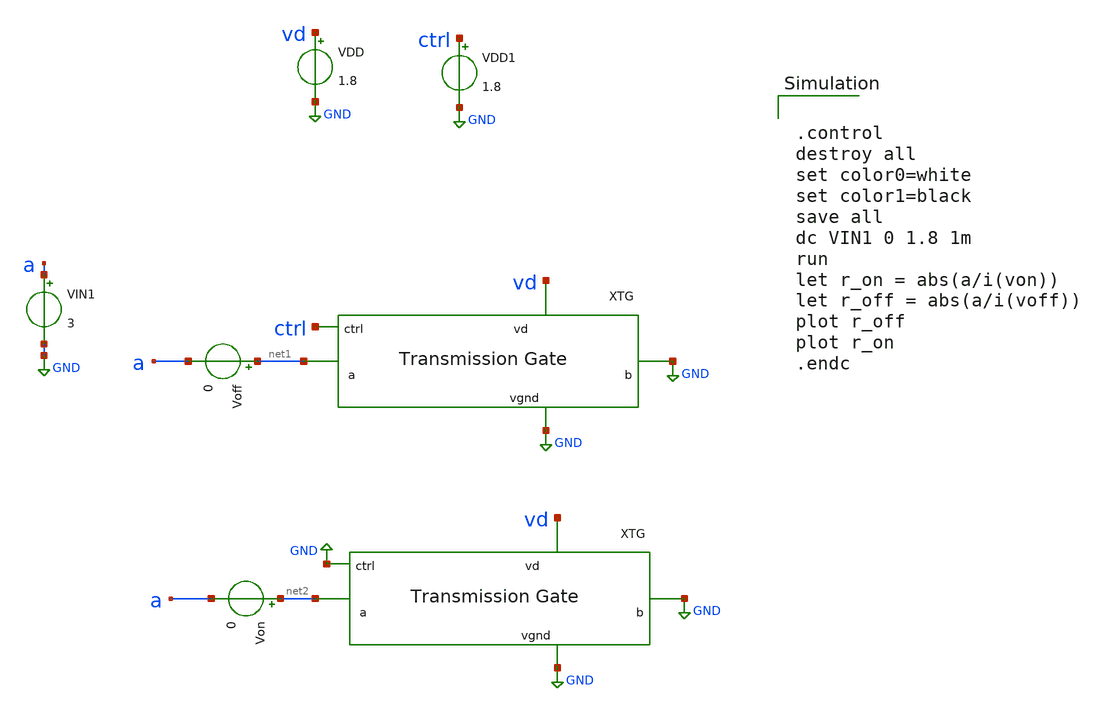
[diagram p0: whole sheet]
** sch_path: xschem/tg-tb-dc.sch
**.subckt tg-tb-dc
VIN1 a GND 3
VDD vd GND 1.8
x1 ctrl vd GND GND net1 tg
VDD1 ctrl GND 1.8
x2 GND vd GND GND net2 tg
Voff net1 a 0
Von net2 a 0
**** begin user architecture code


.control
destroy all
set color0=white
set color1=black
save all
dc VIN1 0 1.8 1m
run
let r_on = abs(a/i(von))
let r_off = abs(a/i(voff))
plot r_off
plot r_on
.endc

 .lib $::SKYWATER_MODELS/sky130.lib.spice tt
.include $::SKYWATER_STDCELLS/sky130_fd_sc_hd.spice

**** end user architecture code
**.ends

* expanding   symbol:  projects/dpga-ieee-sscs-contest/xschem/tg.sym # of pins=5
** sym_path: projects/dpga-ieee-sscs-contest/xschem/tg.sym
** sch_path: projects/dpga-ieee-sscs-contest/xschem/tg.sch
.subckt tg ctrl vd b vgnd a
*.iopin vd
*.iopin vgnd
*.iopin b
*.iopin a
*.ipin ctrl
XM2 b nctrl a vd sky130_fd_pr__pfet_01v8 L=0.15 W=60 nf=12 ad='int((nf+1)/2) * W/nf * 0.29' as='int((nf+2)/2) * W/nf * 0.29'
+ pd='2*int((nf+1)/2) * (W/nf + 0.29)' ps='2*int((nf+2)/2) * (W/nf + 0.29)' nrd='0.29 / W' nrs='0.29 / W'
+ sa=0 sb=0 sd=0 mult=1 m=1
XM1 a ctrl b vgnd sky130_fd_pr__nfet_01v8 L=0.15 W=60 nf=12 ad='int((nf+1)/2) * W/nf * 0.29' as='int((nf+2)/2) * W/nf * 0.29'
+ pd='2*int((nf+1)/2) * (W/nf + 0.29)' ps='2*int((nf+2)/2) * (W/nf + 0.29)' nrd='0.29 / W' nrs='0.29 / W'
+ sa=0 sb=0 sd=0 mult=1 m=1
XM3 nctrl ctrl vgnd vgnd sky130_fd_pr__nfet_01v8 L=0.15 W=1 nf=1 ad='int((nf+1)/2) * W/nf * 0.29' as='int((nf+2)/2) * W/nf * 0.29'
+ pd='2*int((nf+1)/2) * (W/nf + 0.29)' ps='2*int((nf+2)/2) * (W/nf + 0.29)' nrd='0.29 / W' nrs='0.29 / W'
+ sa=0 sb=0 sd=0 mult=1 m=1
XM4 nctrl ctrl vd vd sky130_fd_pr__pfet_01v8 L=0.15 W=3 nf=1 ad='int((nf+1)/2) * W/nf * 0.29' as='int((nf+2)/2) * W/nf * 0.29'
+ pd='2*int((nf+1)/2) * (W/nf + 0.29)' ps='2*int((nf+2)/2) * (W/nf + 0.29)' nrd='0.29 / W' nrs='0.29 / W'
+ sa=0 sb=0 sd=0 mult=1 m=1
.ends

.GLOBAL GND
.end
